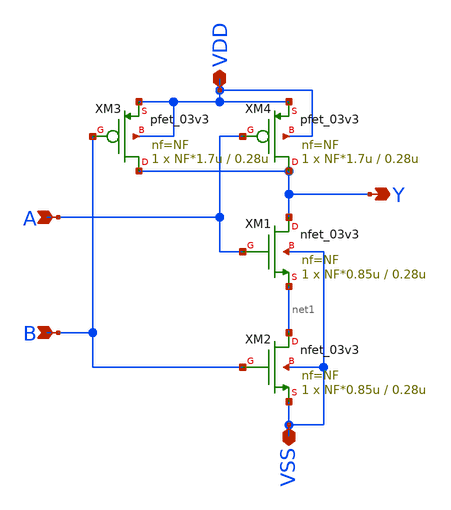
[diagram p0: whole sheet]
** sch_path: xschem_lib/DFFRAM_full_custom/nand.sch
**.subckt nand Y A VDD VSS B
*.opin Y
*.ipin A
*.iopin VDD
*.iopin VSS
*.ipin B
XM2 net1 B VSS VSS nfet_03v3 L=0.28u W=NF*0.85u nf=NF ad='int((nf+1)/2) * W/nf * 0.18u' as='int((nf+2)/2) * W/nf * 0.18u'
+ pd='2*int((nf+1)/2) * (W/nf + 0.18u)' ps='2*int((nf+2)/2) * (W/nf + 0.18u)' nrd='0.18u / W' nrs='0.18u / W'
+ sa=0 sb=0 sd=0 m=1
XM3 Y B VDD VDD pfet_03v3 L=0.28u W=NF*1.7u nf=NF ad='int((nf+1)/2) * W/nf * 0.18u' as='int((nf+2)/2) * W/nf * 0.18u'
+ pd='2*int((nf+1)/2) * (W/nf + 0.18u)' ps='2*int((nf+2)/2) * (W/nf + 0.18u)' nrd='0.18u / W' nrs='0.18u / W'
+ sa=0 sb=0 sd=0 m=1
XM4 Y A VDD VDD pfet_03v3 L=0.28u W=NF*1.7u nf=NF ad='int((nf+1)/2) * W/nf * 0.18u' as='int((nf+2)/2) * W/nf * 0.18u'
+ pd='2*int((nf+1)/2) * (W/nf + 0.18u)' ps='2*int((nf+2)/2) * (W/nf + 0.18u)' nrd='0.18u / W' nrs='0.18u / W'
+ sa=0 sb=0 sd=0 m=1
XM1 Y A net1 VSS nfet_03v3 L=0.28u W=NF*0.85u nf=NF ad='int((nf+1)/2) * W/nf * 0.18u' as='int((nf+2)/2) * W/nf * 0.18u'
+ pd='2*int((nf+1)/2) * (W/nf + 0.18u)' ps='2*int((nf+2)/2) * (W/nf + 0.18u)' nrd='0.18u / W' nrs='0.18u / W'
+ sa=0 sb=0 sd=0 m=1
**.ends
.end
